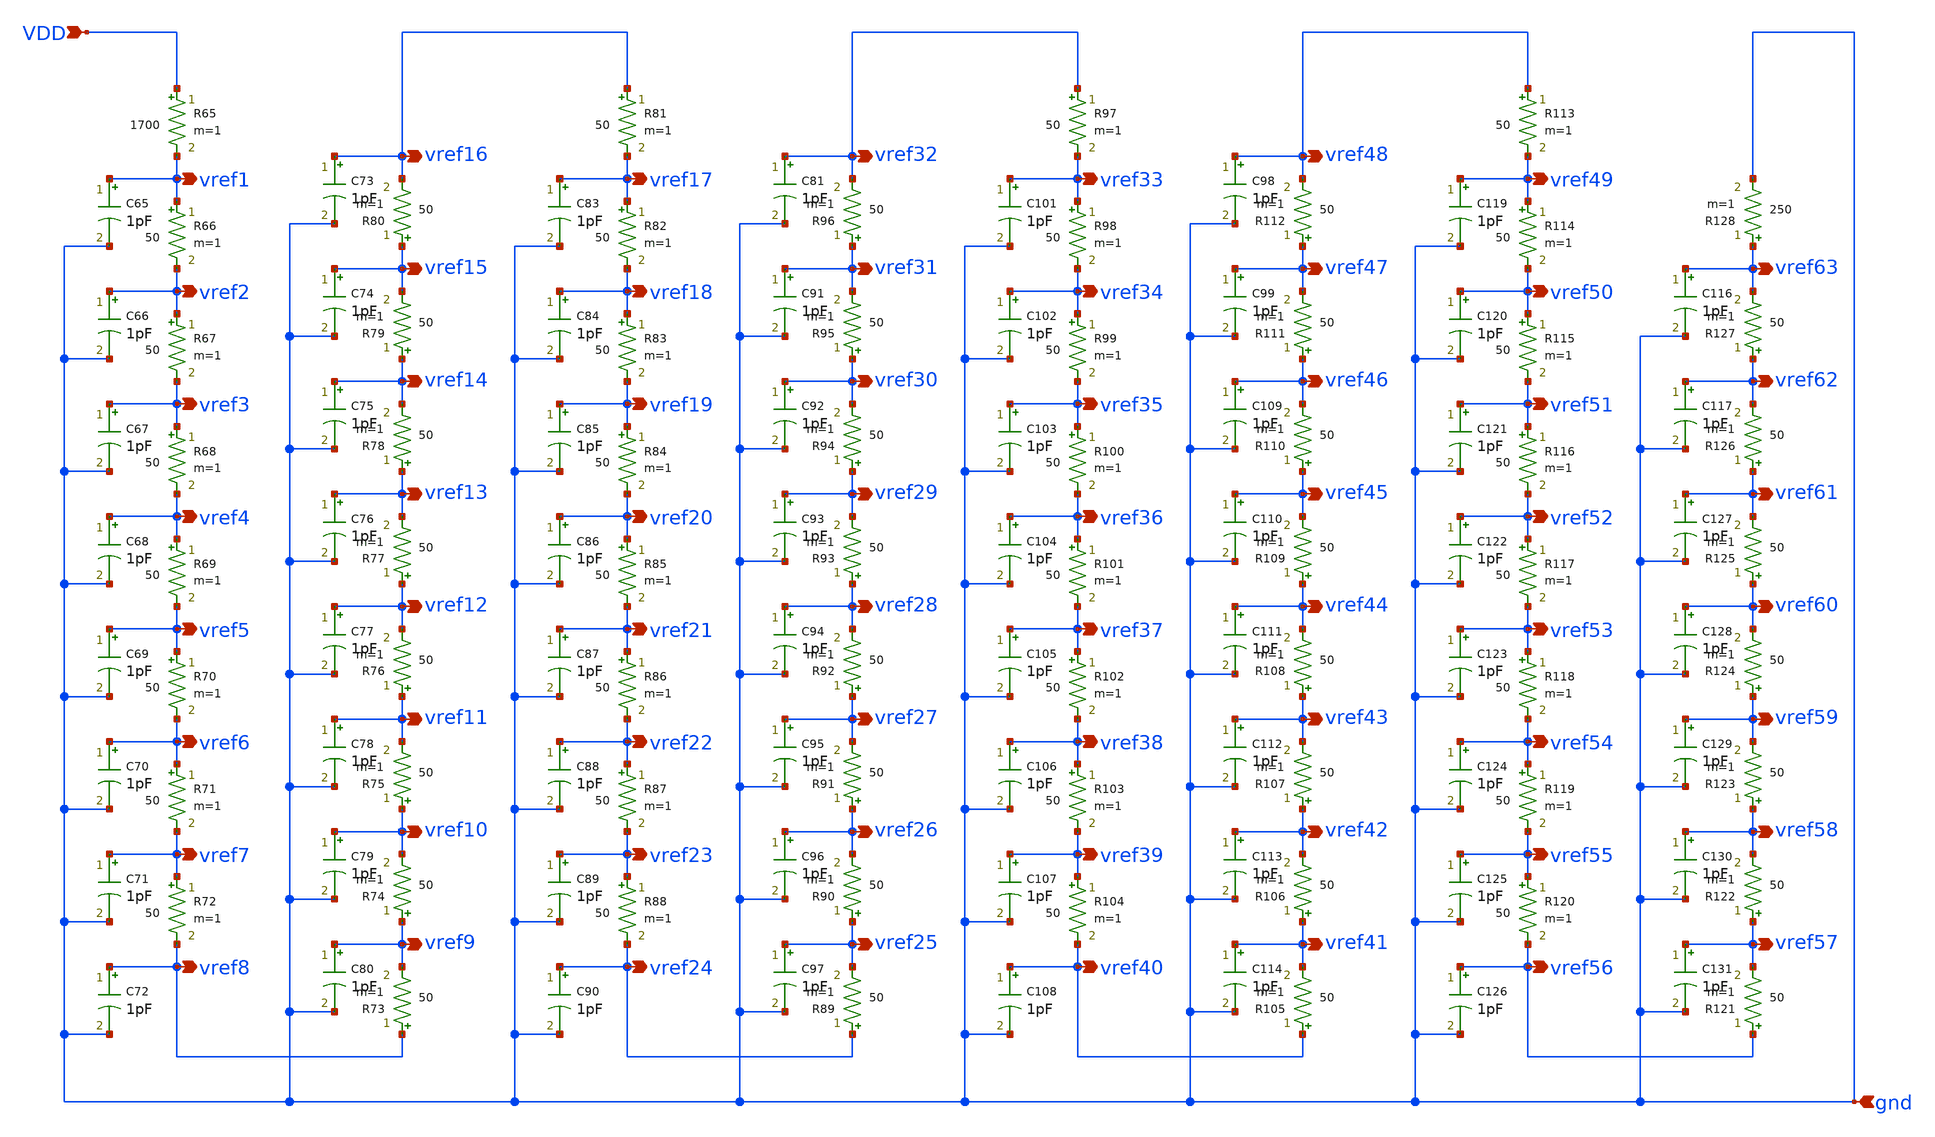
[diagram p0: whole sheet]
** sch_path: ladder_6bit.sch
**.subckt ladder_6bit vref9 vref10 vref11 vref12 vref13 vref14 vref16 vref17 vref18 vref19 vref20
*+ vref21 vref15 vref23 vref24 vref25 vref26 vref27 vref28 vref22 vref30 vref31 vref32 vref33 vref34 vref35
*+ vref29 vref37 vref38 vref39 vref40 vref41 vref42 vref36 vref44 vref45 vref46 vref47 vref48 vref49 vref43
*+ vref51 vref52 vref53 vref54 vref55 vref56 vref50 vref57 vref58 vref59 vref60 vref61 vref62 vref63 VDD gnd
*+ vref2 vref3 vref4 vref5 vref6 vref7 vref1 vref8
*.opin vref9
*.opin vref10
*.opin vref11
*.opin vref12
*.opin vref13
*.opin vref14
*.opin vref16
*.opin vref17
*.opin vref18
*.opin vref19
*.opin vref20
*.opin vref21
*.opin vref15
*.opin vref23
*.opin vref24
*.opin vref25
*.opin vref26
*.opin vref27
*.opin vref28
*.opin vref22
*.opin vref30
*.opin vref31
*.opin vref32
*.opin vref33
*.opin vref34
*.opin vref35
*.opin vref29
*.opin vref37
*.opin vref38
*.opin vref39
*.opin vref40
*.opin vref41
*.opin vref42
*.opin vref36
*.opin vref44
*.opin vref45
*.opin vref46
*.opin vref47
*.opin vref48
*.opin vref49
*.opin vref43
*.opin vref51
*.opin vref52
*.opin vref53
*.opin vref54
*.opin vref55
*.opin vref56
*.opin vref50
*.opin vref57
*.opin vref58
*.opin vref59
*.opin vref60
*.opin vref61
*.opin vref62
*.opin vref63
*.ipin VDD
*.ipin gnd
*.opin vref2
*.opin vref3
*.opin vref4
*.opin vref5
*.opin vref6
*.opin vref7
*.opin vref1
*.opin vref8
R65 VDD vref1 1700 m=1
R66 vref1 vref2 50 m=1
R67 vref2 vref3 50 m=1
R68 vref3 vref4 50 m=1
R69 vref4 vref5 50 m=1
R70 vref5 vref6 50 m=1
R71 vref6 vref7 50 m=1
R72 vref7 vref8 50 m=1
C65 vref1 gnd 1pF m=1
C66 vref2 gnd 1pF m=1
C67 vref3 gnd 1pF m=1
C68 vref4 gnd 1pF m=1
C69 vref5 gnd 1pF m=1
C70 vref6 gnd 1pF m=1
C71 vref7 gnd 1pF m=1
C72 vref8 gnd 1pF m=1
R81 vref16 vref17 50 m=1
R82 vref17 vref18 50 m=1
R83 vref18 vref19 50 m=1
R84 vref19 vref20 50 m=1
R85 vref20 vref21 50 m=1
R86 vref21 vref22 50 m=1
R87 vref22 vref23 50 m=1
R88 vref23 vref24 50 m=1
C83 vref17 gnd 1pF m=1
C84 vref18 gnd 1pF m=1
C85 vref19 gnd 1pF m=1
C86 vref20 gnd 1pF m=1
C87 vref21 gnd 1pF m=1
C88 vref22 gnd 1pF m=1
C89 vref23 gnd 1pF m=1
C90 vref24 gnd 1pF m=1
R97 vref32 vref33 50 m=1
R98 vref33 vref34 50 m=1
R99 vref34 vref35 50 m=1
R100 vref35 vref36 50 m=1
R101 vref36 vref37 50 m=1
R102 vref37 vref38 50 m=1
R103 vref38 vref39 50 m=1
R104 vref39 vref40 50 m=1
C101 vref33 gnd 1pF m=1
C102 vref34 gnd 1pF m=1
C103 vref35 gnd 1pF m=1
C104 vref36 gnd 1pF m=1
C105 vref37 gnd 1pF m=1
C106 vref38 gnd 1pF m=1
C107 vref39 gnd 1pF m=1
C108 vref40 gnd 1pF m=1
R113 vref48 vref49 50 m=1
R114 vref49 vref50 50 m=1
R115 vref50 vref51 50 m=1
R116 vref51 vref52 50 m=1
R117 vref52 vref53 50 m=1
R118 vref53 vref54 50 m=1
R119 vref54 vref55 50 m=1
R120 vref55 vref56 50 m=1
C119 vref49 gnd 1pF m=1
C120 vref50 gnd 1pF m=1
C121 vref51 gnd 1pF m=1
C122 vref52 gnd 1pF m=1
C123 vref53 gnd 1pF m=1
C124 vref54 gnd 1pF m=1
C125 vref55 gnd 1pF m=1
C126 vref56 gnd 1pF m=1
R73 vref8 vref9 50 m=1
R74 vref9 vref10 50 m=1
R75 vref10 vref11 50 m=1
R76 vref11 vref12 50 m=1
R77 vref12 vref13 50 m=1
R78 vref13 vref14 50 m=1
R79 vref14 vref15 50 m=1
R80 vref15 vref16 50 m=1
R89 vref24 vref25 50 m=1
R90 vref25 vref26 50 m=1
R91 vref26 vref27 50 m=1
R92 vref27 vref28 50 m=1
R93 vref28 vref29 50 m=1
R94 vref29 vref30 50 m=1
R95 vref30 vref31 50 m=1
R96 vref31 vref32 50 m=1
R105 vref40 vref41 50 m=1
R106 vref41 vref42 50 m=1
R107 vref42 vref43 50 m=1
R108 vref43 vref44 50 m=1
R109 vref44 vref45 50 m=1
R110 vref45 vref46 50 m=1
R111 vref46 vref47 50 m=1
R112 vref47 vref48 50 m=1
C116 vref63 gnd 1pF m=1
C117 vref62 gnd 1pF m=1
C127 vref61 gnd 1pF m=1
C128 vref60 gnd 1pF m=1
C129 vref59 gnd 1pF m=1
C130 vref58 gnd 1pF m=1
C131 vref57 gnd 1pF m=1
R121 vref56 vref57 50 m=1
R122 vref57 vref58 50 m=1
R123 vref58 vref59 50 m=1
R124 vref59 vref60 50 m=1
R125 vref60 vref61 50 m=1
R126 vref61 vref62 50 m=1
R127 vref62 vref63 50 m=1
R128 vref63 gnd 250 m=1
C98 vref48 gnd 1pF m=1
C99 vref47 gnd 1pF m=1
C109 vref46 gnd 1pF m=1
C110 vref45 gnd 1pF m=1
C111 vref44 gnd 1pF m=1
C112 vref43 gnd 1pF m=1
C113 vref42 gnd 1pF m=1
C114 vref41 gnd 1pF m=1
C81 vref32 gnd 1pF m=1
C91 vref31 gnd 1pF m=1
C92 vref30 gnd 1pF m=1
C93 vref29 gnd 1pF m=1
C94 vref28 gnd 1pF m=1
C95 vref27 gnd 1pF m=1
C96 vref26 gnd 1pF m=1
C97 vref25 gnd 1pF m=1
C73 vref16 gnd 1pF m=1
C74 vref15 gnd 1pF m=1
C75 vref14 gnd 1pF m=1
C76 vref13 gnd 1pF m=1
C77 vref12 gnd 1pF m=1
C78 vref11 gnd 1pF m=1
C79 vref10 gnd 1pF m=1
C80 vref9 gnd 1pF m=1
**.ends
.end
